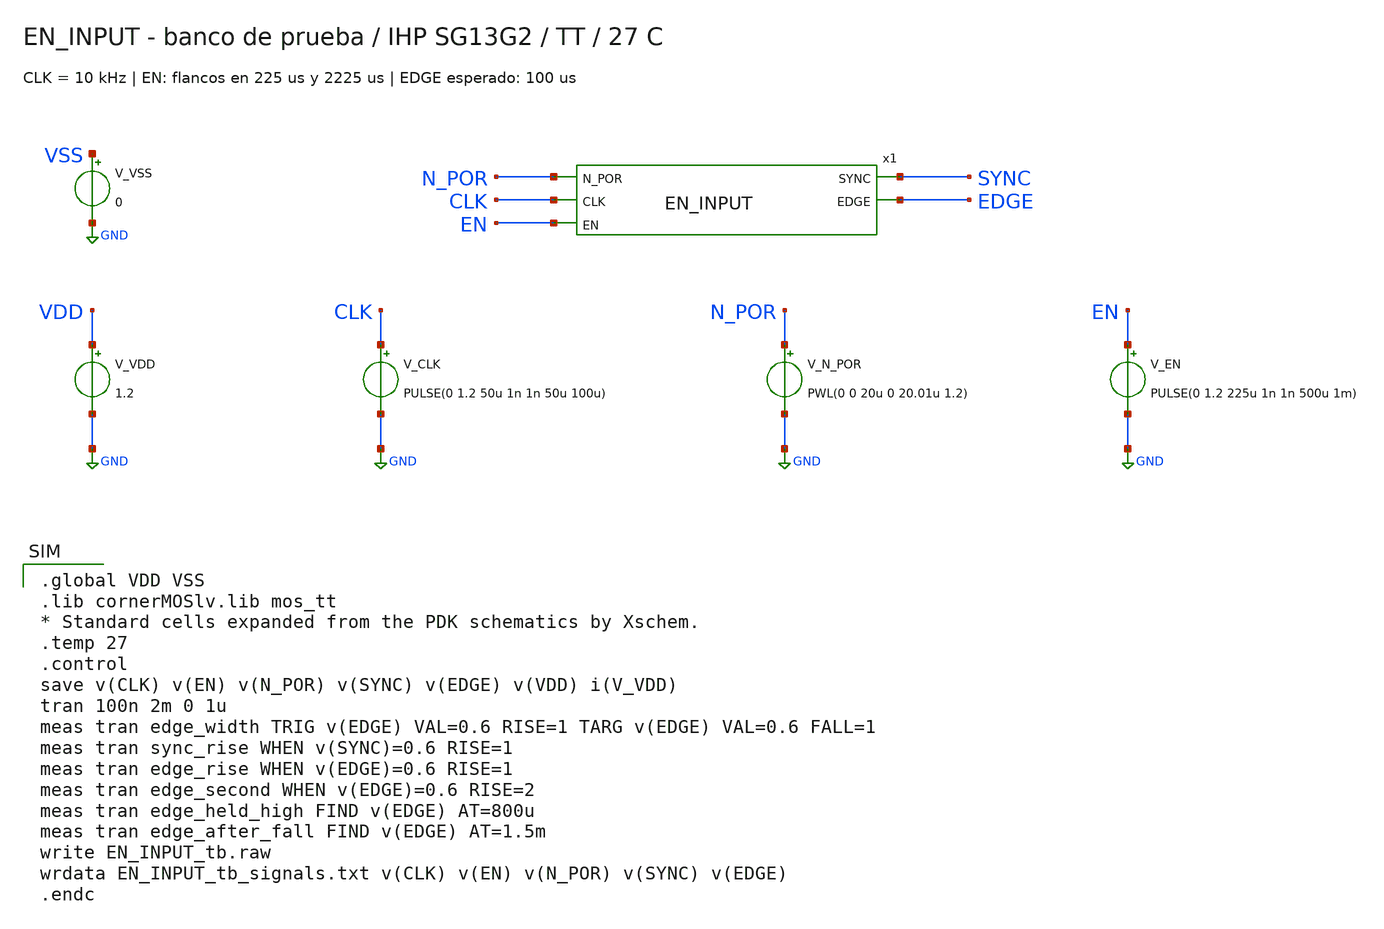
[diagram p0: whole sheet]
** sch_path: design/blocks/enable_input/schematic/EN_INPUT_tb.sch
**.subckt EN_INPUT_tb
x1 N_POR CLK SYNC EN EDGE EN_INPUT
V_VDD VDD GND 1.2
V_CLK CLK GND PULSE(0 1.2 50u 1n 1n 50u 100u)
V_N_POR N_POR GND PWL(0 0 20u 0 20.01u 1.2)
V_EN EN GND PULSE(0 1.2 225u 1n 1n 500u 1m)
V_VSS VSS GND 0
**** begin user architecture code

.global VDD VSS
.lib cornerMOSlv.lib mos_tt
* Standard cells expanded from the PDK schematics by Xschem.
.temp 27
.control
save v(CLK) v(EN) v(N_POR) v(SYNC) v(EDGE) v(VDD) i(V_VDD)
tran 100n 2m 0 1u
meas tran edge_width TRIG v(EDGE) VAL=0.6 RISE=1 TARG v(EDGE) VAL=0.6 FALL=1
meas tran sync_rise WHEN v(SYNC)=0.6 RISE=1
meas tran edge_rise WHEN v(EDGE)=0.6 RISE=1
meas tran edge_second WHEN v(EDGE)=0.6 RISE=2
meas tran edge_held_high FIND v(EDGE) AT=800u
meas tran edge_after_fall FIND v(EDGE) AT=1.5m
write EN_INPUT_tb.raw
wrdata EN_INPUT_tb_signals.txt v(CLK) v(EN) v(N_POR) v(SYNC) v(EDGE)
.endc

**** end user architecture code
**.ends
.GLOBAL GND
.end
